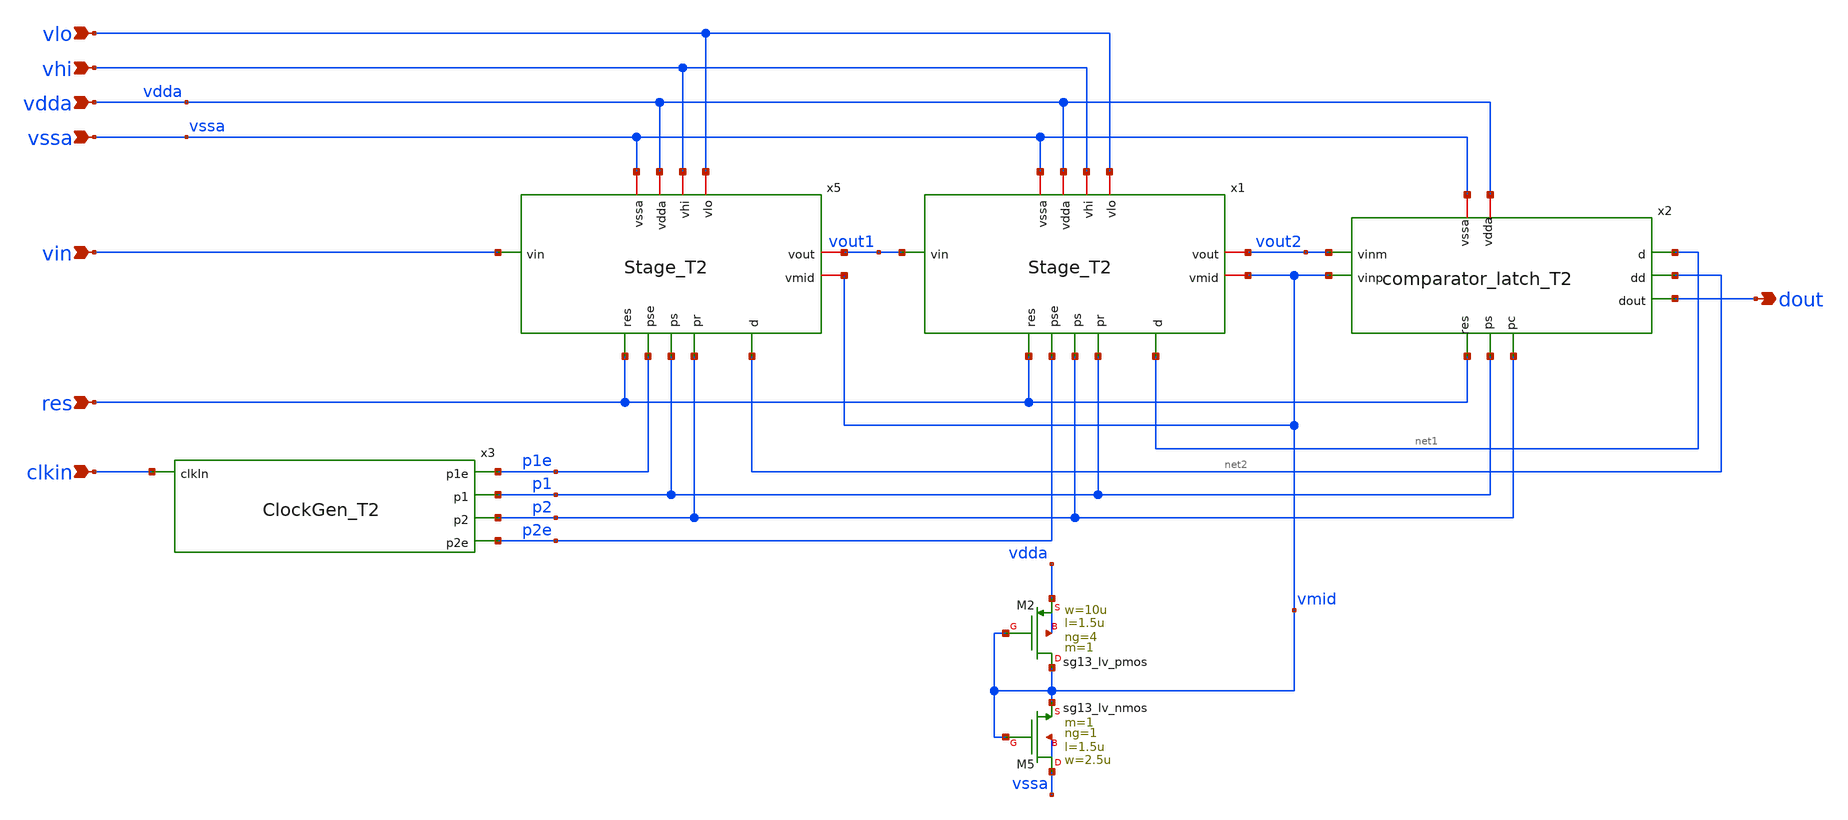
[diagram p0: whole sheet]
** sch_path: 5_Design/4_Layout/Team 2 - Transformer Monster Tractors/xschem/IDSM2_Transistorized_T2.sch
**.subckt IDSM2_Transistorized_T2 clkin res dout vlo vssa vhi vdda vin
*.ipin clkin
*.ipin res
*.opin dout
*.ipin vlo
*.ipin vssa
*.ipin vhi
*.ipin vdda
*.ipin vin
XM2 vmid vmid vdda vdda sg13_lv_pmos w=10u l=1.5u ng=4 m=1 mm_ok=1
XM5 vssa vmid vmid vssa sg13_lv_nmos w=2.5u l=1.5u ng=1 m=1 mm_ok=1
x5 vmid res p1e p1 p2 vhi vdda vin vssa net2 vlo vout1 Stage_T2
x2 vdda p2 net1 net2 dout vmid res vssa p1 vout2 comparator_latch_T2
x3 p1e clkin p1 p2 p2e ClockGen_T2
x1 vmid res p2e p2 p1 vhi vdda vout1 vssa net1 vlo vout2 Stage_T2
**.ends
.end
